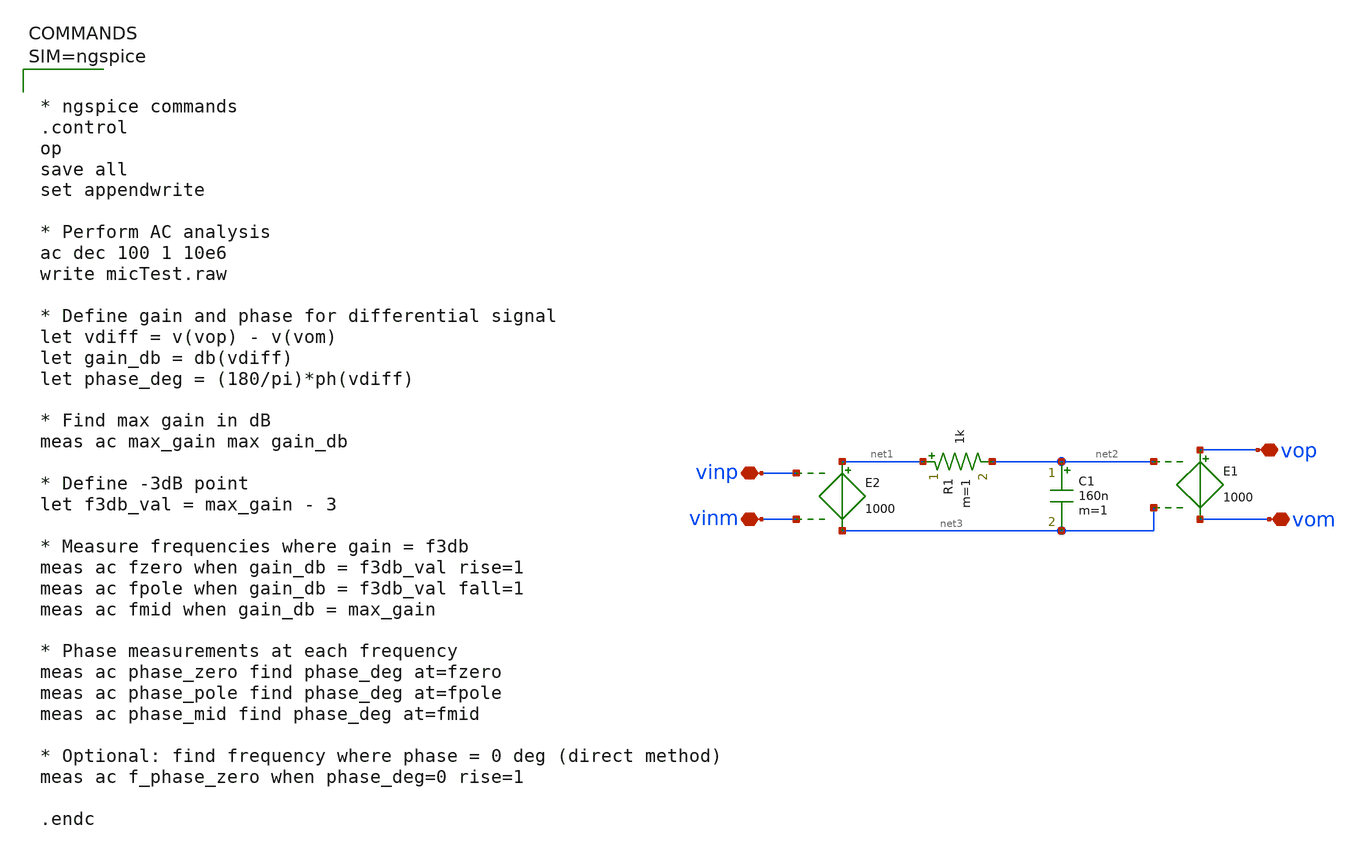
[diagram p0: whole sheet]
** sch_path: xschem/day6_scem.sch
**.subckt day6_scem vop vom vinm vinp
*.iopin vop
*.iopin vom
*.iopin vinm
*.iopin vinp
E1 vop vom net2 net3 1000
E2 net1 net3 vinp vinm 1000
C1 net2 net3 160n m=1
R1 net1 net2 1k m=1
**** begin user architecture code



* ngspice commands
.control
op
save all
set appendwrite

* Perform AC analysis
ac dec 100 1 10e6
write micTest.raw

* Define gain and phase for differential signal
let vdiff = v(vop) - v(vom)
let gain_db = db(vdiff)
let phase_deg = (180/pi)*ph(vdiff)

* Find max gain in dB
meas ac max_gain max gain_db

* Define -3dB point
let f3db_val = max_gain - 3

* Measure frequencies where gain = f3db
meas ac fzero when gain_db = f3db_val rise=1
meas ac fpole when gain_db = f3db_val fall=1
meas ac fmid when gain_db = max_gain

* Phase measurements at each frequency
meas ac phase_zero find phase_deg at=fzero
meas ac phase_pole find phase_deg at=fpole
meas ac phase_mid find phase_deg at=fmid

* Optional: find frequency where phase = 0 deg (direct method)
meas ac f_phase_zero when phase_deg=0 rise=1

.endc



**** end user architecture code
**.ends
.end
